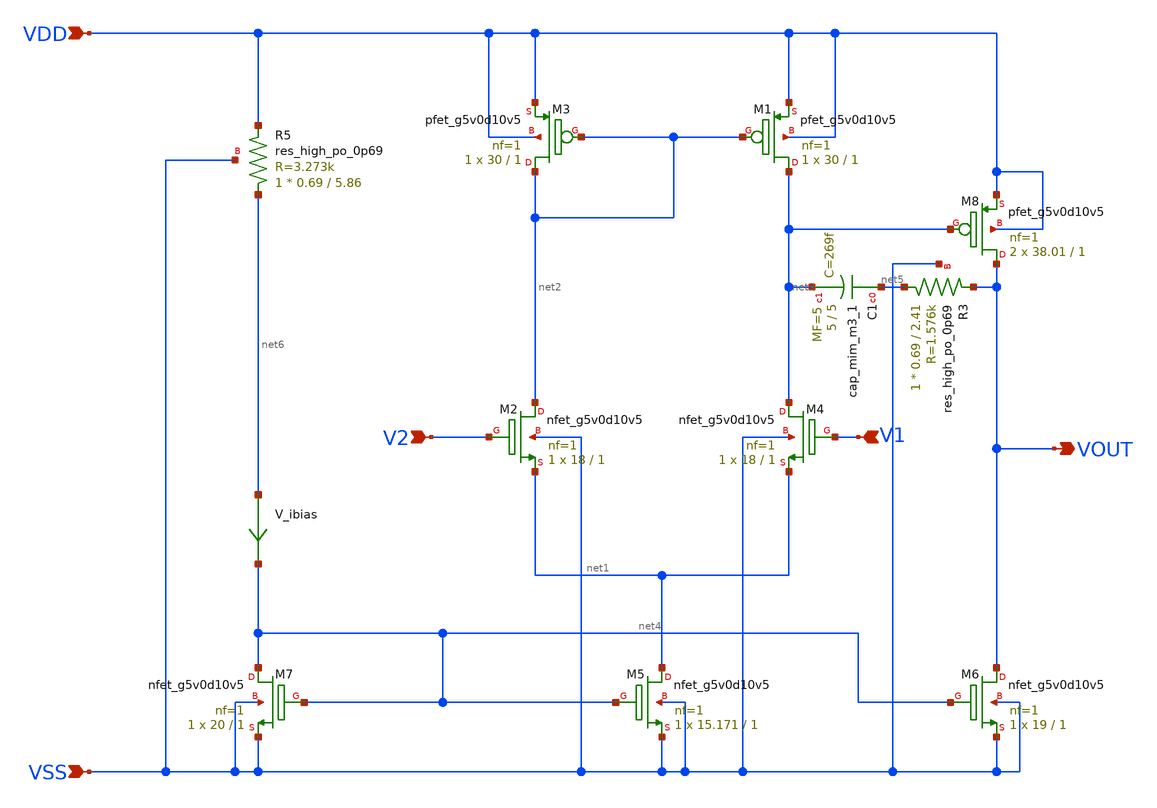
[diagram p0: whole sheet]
** sch_path: xschem/opamp_v2_backup.sch
**.subckt opamp_v2_backup VSS VDD V2 V1 VOUT
*.ipin VSS
*.ipin VDD
*.ipin V2
*.ipin V1
*.opin VOUT
XM2 net2 V2 net1 VSS sky130_fd_pr__nfet_g5v0d10v5 L=1 W=18 nf=1 ad='int((nf+1)/2) * W/nf * 0.29' as='int((nf+2)/2) * W/nf * 0.29'
+ pd='2*int((nf+1)/2) * (W/nf + 0.29)' ps='2*int((nf+2)/2) * (W/nf + 0.29)' nrd='0.29 / W' nrs='0.29 / W'
+ sa=0 sb=0 sd=0 mult=1 m=1
XM1 net3 net2 VDD VDD sky130_fd_pr__pfet_g5v0d10v5 L=1 W=30 nf=1 ad='int((nf+1)/2) * W/nf * 0.29' as='int((nf+2)/2) * W/nf * 0.29'
+ pd='2*int((nf+1)/2) * (W/nf + 0.29)' ps='2*int((nf+2)/2) * (W/nf + 0.29)' nrd='0.29 / W' nrs='0.29 / W'
+ sa=0 sb=0 sd=0 mult=1 m=1
XM4 net3 V1 net1 VSS sky130_fd_pr__nfet_g5v0d10v5 L=1 W=18 nf=1 ad='int((nf+1)/2) * W/nf * 0.29' as='int((nf+2)/2) * W/nf * 0.29'
+ pd='2*int((nf+1)/2) * (W/nf + 0.29)' ps='2*int((nf+2)/2) * (W/nf + 0.29)' nrd='0.29 / W' nrs='0.29 / W'
+ sa=0 sb=0 sd=0 mult=1 m=1
XM5 net1 net4 VSS VSS sky130_fd_pr__nfet_g5v0d10v5 L=1 W=15.171 nf=1 ad='int((nf+1)/2) * W/nf * 0.29'
+ as='int((nf+2)/2) * W/nf * 0.29' pd='2*int((nf+1)/2) * (W/nf + 0.29)' ps='2*int((nf+2)/2) * (W/nf + 0.29)'
+ nrd='0.29 / W' nrs='0.29 / W' sa=0 sb=0 sd=0 mult=1 m=1
XM6 VOUT net4 VSS VSS sky130_fd_pr__nfet_g5v0d10v5 L=1 W=19 nf=1 ad='int((nf+1)/2) * W/nf * 0.29' as='int((nf+2)/2) * W/nf * 0.29'
+ pd='2*int((nf+1)/2) * (W/nf + 0.29)' ps='2*int((nf+2)/2) * (W/nf + 0.29)' nrd='0.29 / W' nrs='0.29 / W'
+ sa=0 sb=0 sd=0 mult=1 m=1
XM7 net4 net4 VSS VSS sky130_fd_pr__nfet_g5v0d10v5 L=1 W=20 nf=1 ad='int((nf+1)/2) * W/nf * 0.29' as='int((nf+2)/2) * W/nf * 0.29'
+ pd='2*int((nf+1)/2) * (W/nf + 0.29)' ps='2*int((nf+2)/2) * (W/nf + 0.29)' nrd='0.29 / W' nrs='0.29 / W'
+ sa=0 sb=0 sd=0 mult=1 m=1
XM3 net2 net2 VDD VDD sky130_fd_pr__pfet_g5v0d10v5 L=1 W=30 nf=1 ad='int((nf+1)/2) * W/nf * 0.29' as='int((nf+2)/2) * W/nf * 0.29'
+ pd='2*int((nf+1)/2) * (W/nf + 0.29)' ps='2*int((nf+2)/2) * (W/nf + 0.29)' nrd='0.29 / W' nrs='0.29 / W'
+ sa=0 sb=0 sd=0 mult=1 m=1
XM8 VOUT net3 VDD VDD sky130_fd_pr__pfet_g5v0d10v5 L=1 W=38.01 nf=1 ad='int((nf+1)/2) * W/nf * 0.29'
+ as='int((nf+2)/2) * W/nf * 0.29' pd='2*int((nf+1)/2) * (W/nf + 0.29)' ps='2*int((nf+2)/2) * (W/nf + 0.29)'
+ nrd='0.29 / W' nrs='0.29 / W' sa=0 sb=0 sd=0 mult=2 m=2
XC1 net5 net3 sky130_fd_pr__cap_mim_m3_1 W=5 L=5 MF=5 m=5
V_ibias net6 net4 0
.save i(v_ibias)
XR5 net6 VDD VSS sky130_fd_pr__res_high_po_0p69 L=5.86 mult=1 m=1
XR3 net5 VOUT VSS sky130_fd_pr__res_high_po_0p69 L=2.41 mult=1 m=1
**.ends
.end
